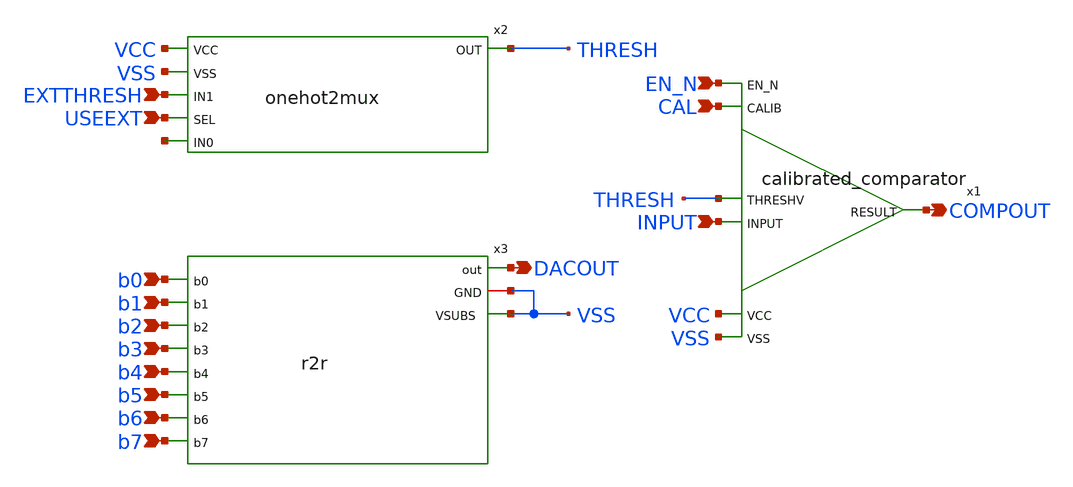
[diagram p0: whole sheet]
** sch_path: ADC_Block.sch
**.subckt ADC_Block USEEXT EXTTHRESH b0 b1 b2 b3 b4 b5 b6 b7 EN_N CAL INPUT DACOUT COMPOUT
*.ipin USEEXT
*.ipin EXTTHRESH
*.ipin b0
*.ipin b1
*.ipin b2
*.ipin b3
*.ipin b4
*.ipin b5
*.ipin b6
*.ipin b7
*.ipin EN_N
*.ipin CAL
*.ipin INPUT
*.opin DACOUT
*.opin COMPOUT
x1 VCC VSS EN_N CAL INPUT THRESH COMPOUT calibrated_comparator
x2 VCC VSS EXTTHRESH USEEXT THRESH net1 onehot2mux
x3 b3 b1 b2 b0 b4 b5 b6 b7 DACOUT VSS VSS r2r
**.ends
.end
